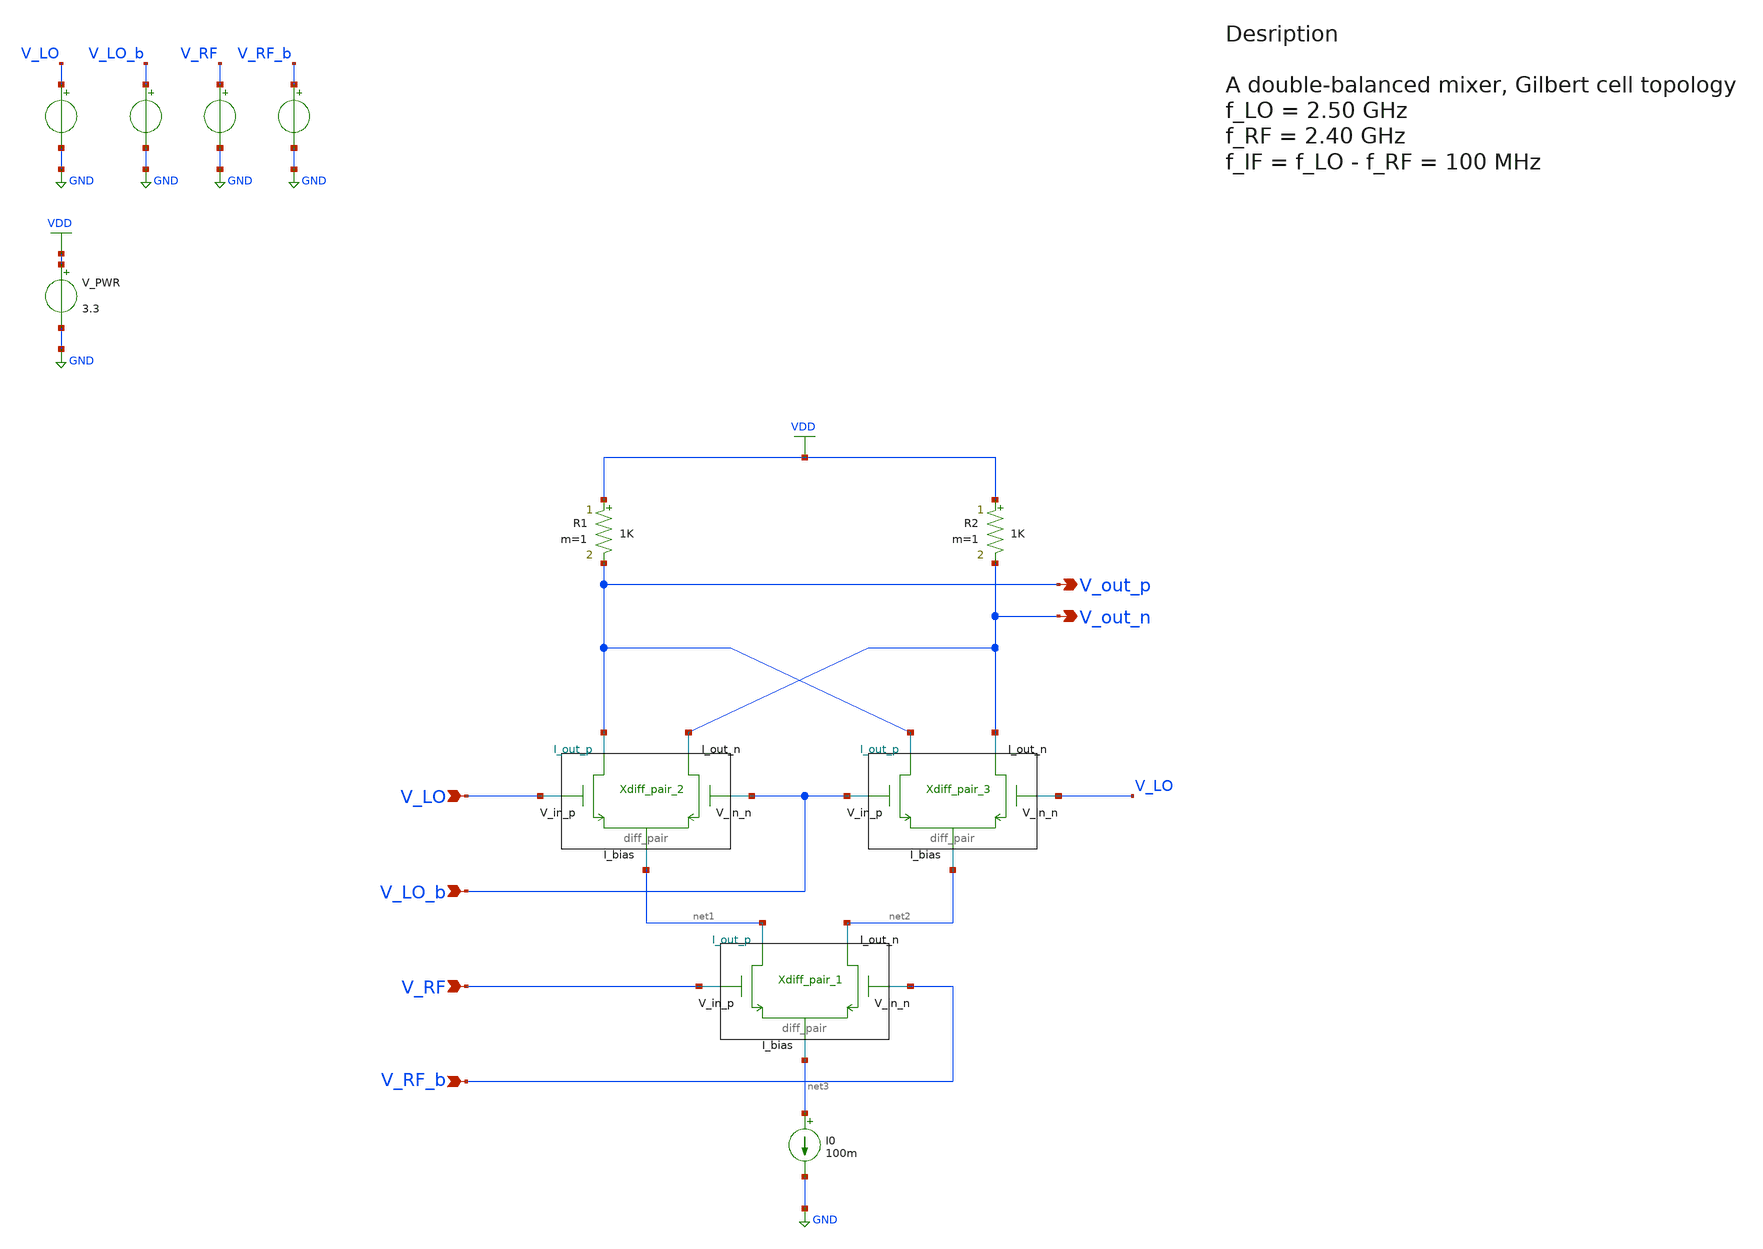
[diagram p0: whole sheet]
** sch_path: src/design_xsch/Gilbert_cell.sch
**.subckt Gilbert_cell V_LO V_LO_b V_RF V_RF_b V_out_p V_out_n
*.ipin V_LO
*.ipin V_LO_b
*.ipin V_RF
*.ipin V_RF_b
*.opin V_out_p
*.opin V_out_n
I0 net3 GND 100m
Xdiff_pair_1 net2 net1 V_RF V_RF_b net3 VSS diff_pair W_neg=0.22u L_neg=0.28u W_pos=2u L_pos=0.28u
+ m=1
Xdiff_pair_2 V_out_n V_out_p V_LO V_LO_b net1 VSS diff_pair W_neg=0.22u L_neg=0.28u W_pos=0.22u
+ L_pos=0.28u m=1
Xdiff_pair_3 V_out_n V_out_p V_LO_b V_LO net2 VSS diff_pair W_neg=0.22u L_neg=0.28u W_pos=0.22u
+ L_pos=0.28u m=1
R1 VDD V_out_p 1K m=1
R2 VDD V_out_n 1K m=1
V_PWR VDD GND 3.3
.save i(v_pwr)
V_LO V_LO GND pulse(0 1.5 0 1p 1p 0.25n 0.5n)
.save i(v_lo)
V_LO_b V_LO_b GND pulse(0 1.5 0 1p 1p 0.25n 0.5n)
.save i(v_lo_b)
V_RF V_RF GND sin( 1 1 1 0 )
.save i(v_rf)
V_RF_b V_RF_b GND sin( 1 1 1 0 0 180 )
.save i(v_rf_b)
**** begin user architecture code

.include $::180MCU_MODELS/design.ngspice
.lib $::180MCU_MODELS/sm141064.ngspice typical



* let sets vectors to a plot, while set sets a variable, globally accessible in .control
.control

    * Set frequency and amplitude variables to proper values from within the control sequence
    * sine-wave LO
    * set cm_lo = 0.5
    * set freq_lo = 2.50G
    * set amp_lo = 0.5
    * alter @V_LO[sin] = [ $cm_lo $amp_lo $freq_lo 0 ]
    * alter @V_LO_b[sin] = [ $cm_lo $amp_lo $freq_lo 0 0 180 ]

    set edge_time_lo = 0.5p
    set freq_lo = 2.50G
    set cm_lo = 1.5
    set amp_lo = 0.25

    set cm_rf  = 1.0
    set freq_rf = 2.40G
    set amp_rf  = 0.2

    let period_lo = 1/$freq_lo
    let half_period_lo = period_lo/2

    * set the parameters to the voltage sources


    alter @V_LO[pulse] = [ ($cm_lo - $amp_lo) ($cm_lo + $amp_lo) 0 $edge_time_lo $edge_time_lo 1/(2
+ * $freq_lo) 1/$freq_lo]
    alter @V_LO_b[pulse] = [ $cm_lo-$amp_lo $cm_lo+$amp_lo $half_period_lo $edge_time_lo
+ $edge_time_lo $half_period_lo $period_lo]
    alter @V_RF[sin] = [ $cm_rf $amp_rf $freq_rf 0 ]
    alter @V_RF_b[sin] = [ $cm_rf $amp_rf $freq_rf 0 0 180 ]

    save all

    * operating point
    op
    write Gilbert_sim.raw

    set appendwrite

    * Transient analysis to observe mixing operation
    tran 1p 10n
    write Gilbert_sim.raw

    * Calculate differential output for conversion gain measurement
    let v_out_diff = v(v_out_p)-v(v_out_n)
    let v_rf_diff = v(v_rf)-v(v_rf_b)

    * Extract IF component at 100MHz using FFT
    linearize v_out_diff v_rf_diff
    let time_step = 10e-12
    let sample_freq = 1/time_step
    let npts = length(v_out_diff)
    let freq_res = sample_freq/npts


    fft v_out_diff v_rf_diff
    * Find frequency bins

    * print everything, sanity check
    set     ; print all available global (?) variables (?)
    setplot ; print all plots
    display ; print variables available in current plot

    let freq_res = tran2.freq_res
    let freq_if = abs( $freq_lo - $freq_rf )

    let if_bin = floor( freq_if/freq_res )
    let rf_bin = floor( $freq_rf/freq_res )

    * Measure conversion gain (power gain from RF to IF)
    let rf_mag = abs(v_rf_diff[rf_bin])
    let if_mag = abs(v_out_diff[if_bin])
    let conversion_gain_db = 20*log10(if_mag/rf_mag)
    print conversion_gain_db

    write Gilbert_sim.raw

.endc


**** end user architecture code
**.ends

* expanding   symbol:  /home/vasil/Downloads/SSCS_PICO_2025/src/design_xsch/diff_pair.sym # of
*+ pins=5
** sym_path: src/design_xsch/diff_pair.sym
** sch_path: src/design_xsch/diff_pair.sch
.subckt diff_pair I_out_n I_out_p V_in_p V_in_n I_bias VSSPIN  mult=1  W_neg=0.22u L_neg=0.28u
+ W_pos=0.22u L_pos=0.28u
*.ipin V_in_p
*.ipin V_in_n
*.iopin I_out_p
*.iopin I_out_n
*.iopin I_bias
XM1 I_out_p V_in_p I_bias VSS nfet_03v3 L=L_pos W=W_pos nf=1 ad='int((nf+1)/2) * W/nf * 0.18u' as='int((nf+2)/2) * W/nf * 0.18u'
+ pd='2*int((nf+1)/2) * (W/nf + 0.18u)' ps='2*int((nf+2)/2) * (W/nf + 0.18u)' nrd='0.18u / W' nrs='0.18u / W'
+ sa=0 sb=0 sd=0 m=mult
XM2 I_out_n V_in_n I_bias VSS nfet_03v3 L=L_neg W=W_neg nf=1 ad='int((nf+1)/2) * W/nf * 0.18u' as='int((nf+2)/2) * W/nf * 0.18u'
+ pd='2*int((nf+1)/2) * (W/nf + 0.18u)' ps='2*int((nf+2)/2) * (W/nf + 0.18u)' nrd='0.18u / W' nrs='0.18u / W'
+ sa=0 sb=0 sd=0 m=mult
.ends

.GLOBAL VDD
.GLOBAL GND
.GLOBAL VSS
.end
